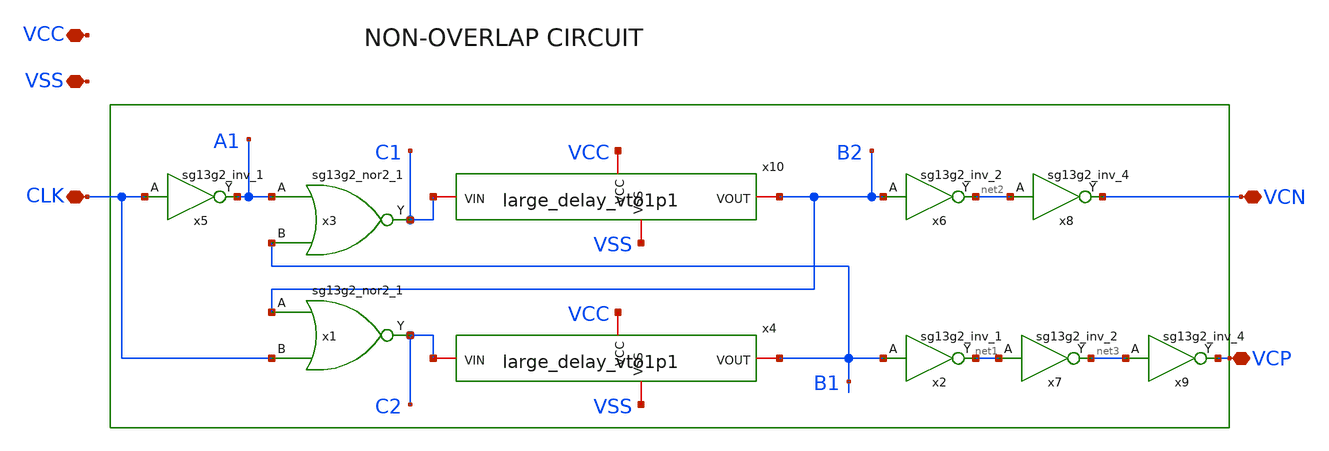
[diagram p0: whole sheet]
** sch_path: xschem/IHP_digital/NOL/NOL_vto1p1.sch
* IHP-GmbH/IHP-Open-PDK/ihp-sg13g2/libs.tech/xschem/sg13g2_stdcells/sg13g2_inv_2.sch:
* Copyright 2023 IHP PDK Authors
* Licensed under the Apache License, Version 2.0 (the "License");
**.subckt NOL_vto1p1 CLK VCP VCN VCC VSS
*.iopin CLK
*.iopin VCP
*.iopin VCN
*.iopin VCC
*.iopin VSS
x5 A1 CLK VCC VSS sg13g2_inv_1
x3 C1 A1 B1 VCC VSS sg13g2_nor2_1
x1 C2 B2 CLK VCC VSS sg13g2_nor2_1
x2 net1 B1 VCC VSS sg13g2_inv_1
x6 net2 B2 VCC VSS sg13g2_inv_2
x7 net3 net1 VCC VSS sg13g2_inv_2
x8 VCN net2 VCC VSS sg13g2_inv_4
x9 VCP net3 VCC VSS sg13g2_inv_4
x10 VCC VSS C1 B2 large_delay_vto1p1
x4 VCC VSS C2 B1 large_delay_vto1p1
**.ends

* expanding   symbol:  sg13g2_stdcells/sg13g2_inv_1.sym # of pins=2
** sym_path: sg13g2_stdcells/sg13g2_inv_1.sym
** sch_path: sg13g2_stdcells/sg13g2_inv_1.sch
.subckt sg13g2_inv_1 Y A VDD VSS
*.opin Y
*.ipin A
*.iopin VDD
*.iopin VSS
XM1 Y A VSS VSS sg13_lv_nmos w=740.00n l=130.00n ng=1 m=1 mm_ok=1
XM2 Y A VDD VDD sg13_lv_pmos w=1.12u l=130.00n ng=1 m=1 mm_ok=1
.ends


* expanding   symbol:  sg13g2_stdcells/sg13g2_nor2_1.sym # of pins=3
** sym_path: sg13g2_stdcells/sg13g2_nor2_1.sym
** sch_path: sg13g2_stdcells/sg13g2_nor2_1.sch
.subckt sg13g2_nor2_1 Y A B VDD VSS
*.opin Y
*.ipin B
*.ipin A
*.iopin VDD
*.iopin VSS
XM1 Y A VSS VSS sg13_lv_nmos w=740.00n l=130.00n ng=1 m=1 mm_ok=1
XM2 Y B VSS VSS sg13_lv_nmos w=740.00n l=130.00n ng=1 m=1 mm_ok=1
XM3 net1 A VDD VDD sg13_lv_pmos w=1.12u l=130.00n ng=1 m=1 mm_ok=1
XM4 Y B net1 VDD sg13_lv_pmos w=1.12u l=130.00n ng=1 m=1 mm_ok=1
.ends


* expanding   symbol:  sg13g2_stdcells/sg13g2_inv_2.sym # of pins=2
** sym_path: sg13g2_stdcells/sg13g2_inv_2.sym
** sch_path: sg13g2_stdcells/sg13g2_inv_2.sch
.subckt sg13g2_inv_2 Y A VDD VSS
*.opin Y
*.ipin A
*.iopin VDD
*.iopin VSS
XM1 Y A VSS VSS sg13_lv_nmos w=1.48u l=130.00n ng=2 m=1 mm_ok=1
XM2 Y A VDD VDD sg13_lv_pmos w=2.24u l=130.00n ng=2 m=1 mm_ok=1
.ends


* expanding   symbol:  sg13g2_stdcells/sg13g2_inv_4.sym # of pins=2
** sym_path: sg13g2_stdcells/sg13g2_inv_4.sym
** sch_path: sg13g2_stdcells/sg13g2_inv_4.sch
.subckt sg13g2_inv_4 Y A VDD VSS
*.ipin A
*.opin Y
*.iopin VDD
*.iopin VSS
XM1 Y A VSS VSS sg13_lv_nmos w=2.96u l=130.00n ng=4 m=1 mm_ok=1
XM2 Y A VDD VDD sg13_lv_pmos w=4.48u l=130.00n ng=4 m=1 mm_ok=1
.ends


* expanding   symbol:
*+  /foss/designs/SSCS-Chipathon-2025_AC3E-Chile-team/xschem/IHP_digital/large_delay/large_delay_vto1p1.sym # of pins=4
** sym_path: xschem/gf180_digital/large_delay/large_delay_vto1p1.sym
** sch_path: xschem/gf180_digital/large_delay/large_delay_vto1p1.sch
.subckt large_delay_vto1p1 VDDd VSSd VIN VOUT
*.iopin VIN
*.iopin VOUT
*.iopin VDDd
*.iopin VSSd
x1 VIN VOUT VDDd VDDd VSSd VSSd gf180mcu_fd_sc_mcu9t5v0__dlyd_1
.ends

.end
